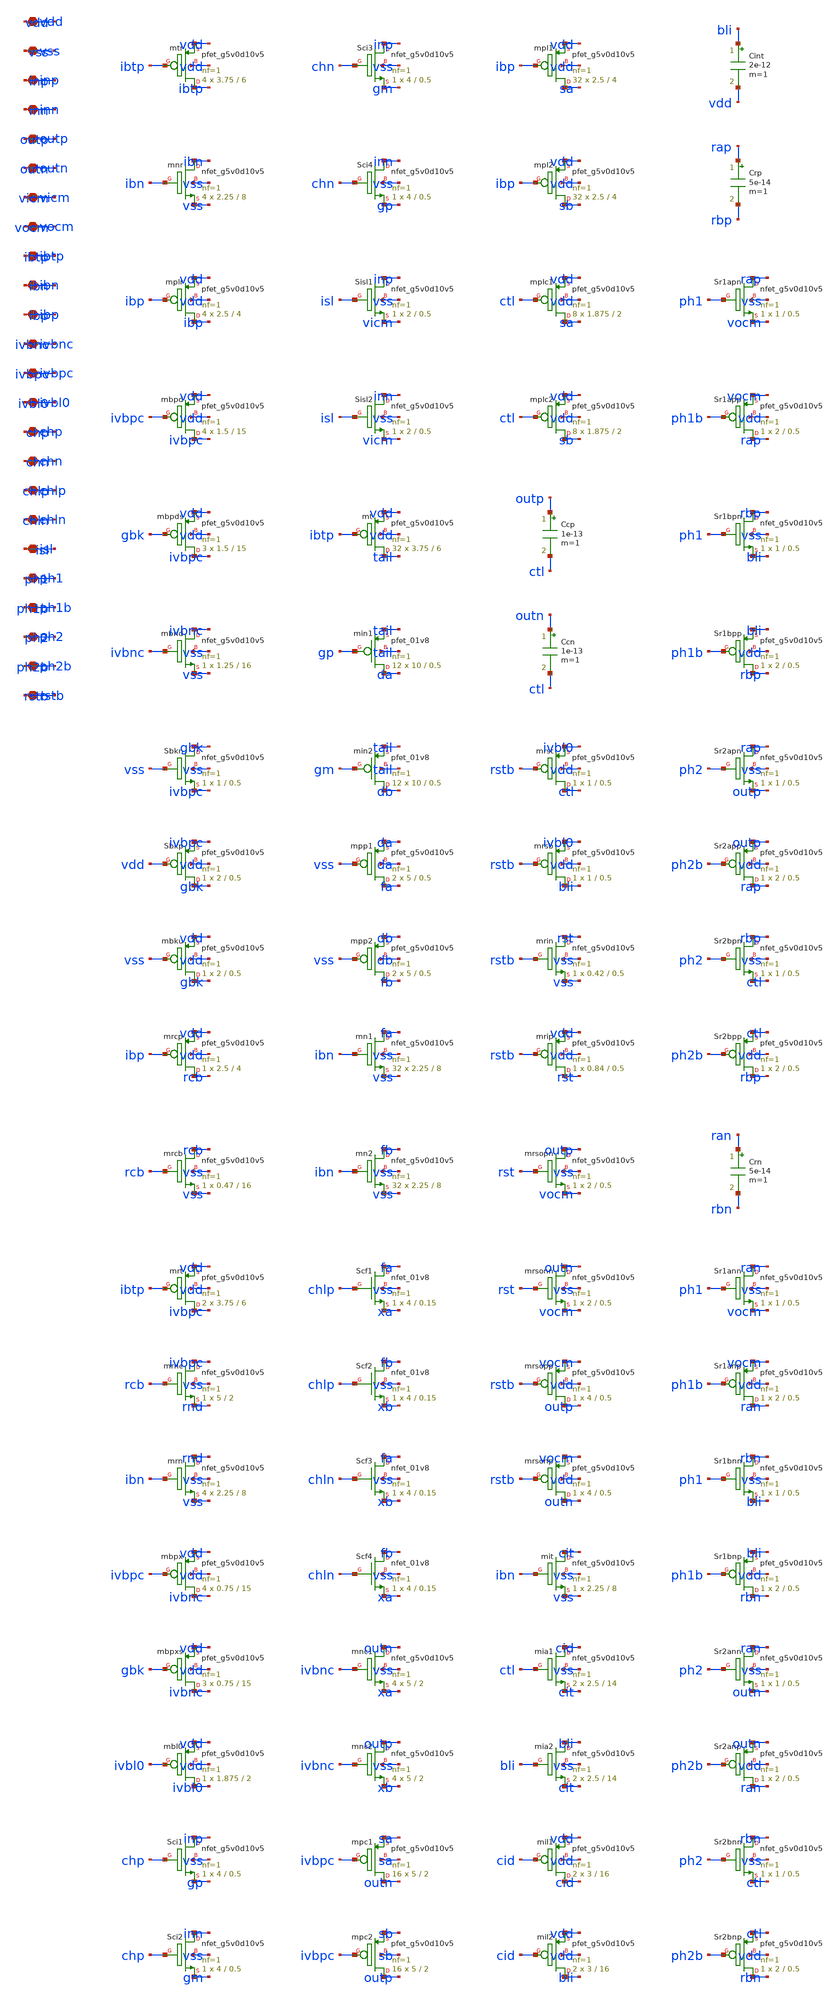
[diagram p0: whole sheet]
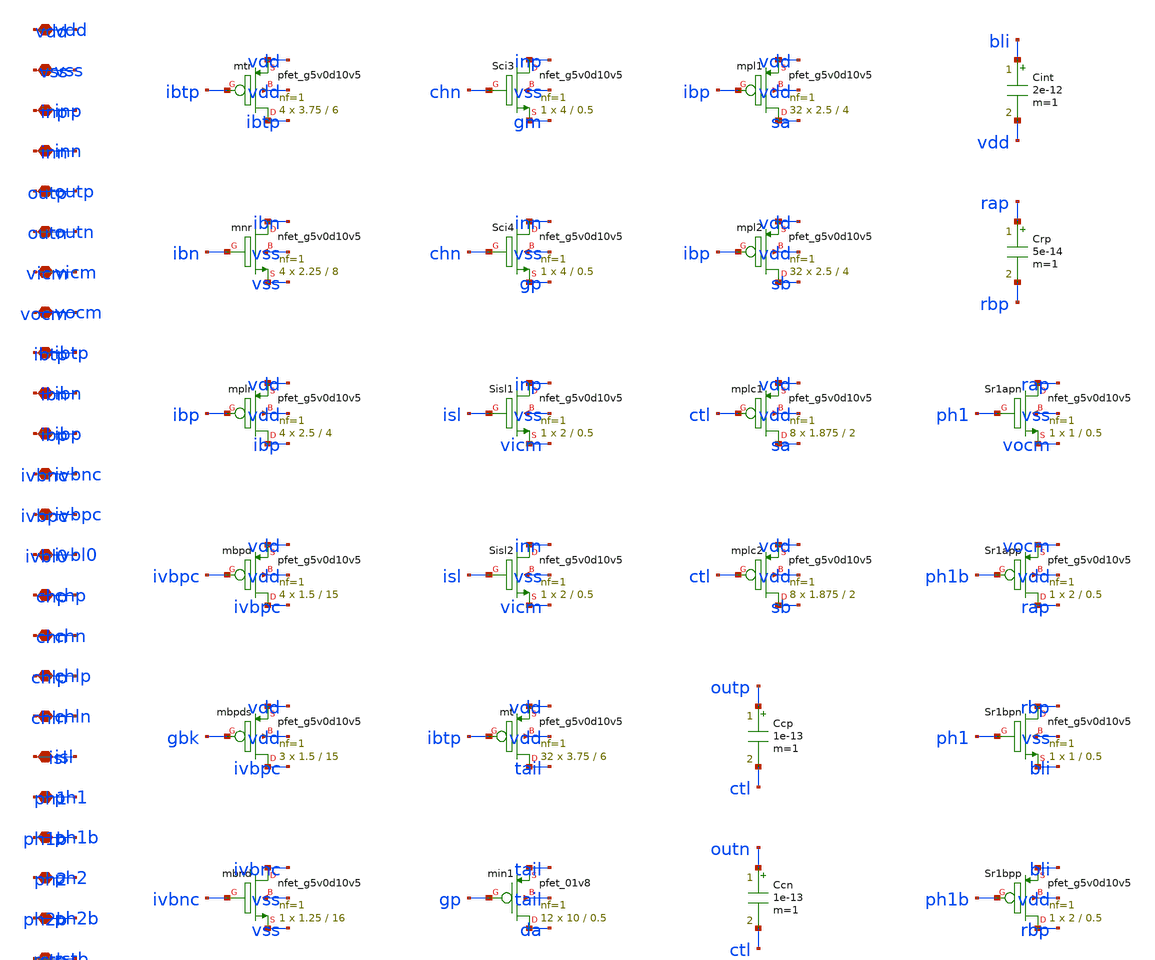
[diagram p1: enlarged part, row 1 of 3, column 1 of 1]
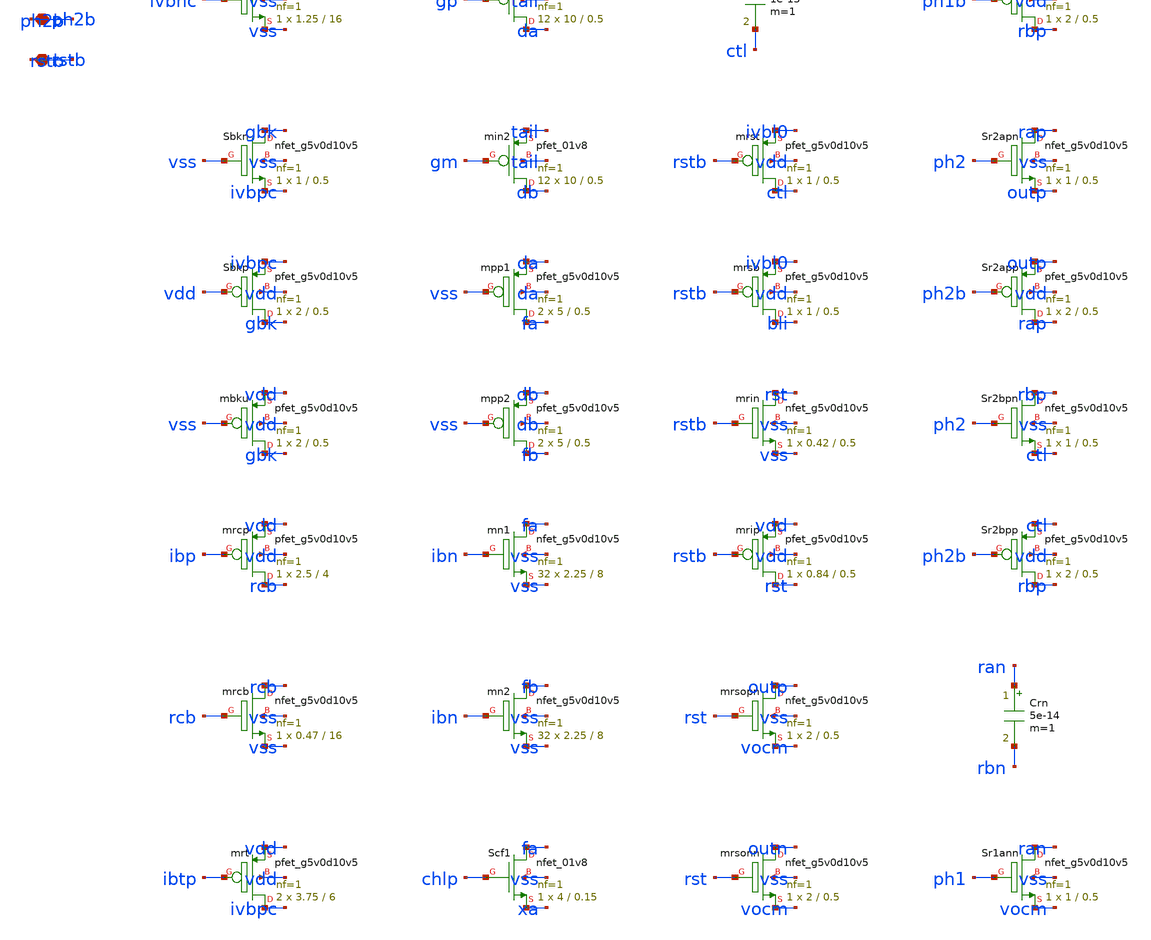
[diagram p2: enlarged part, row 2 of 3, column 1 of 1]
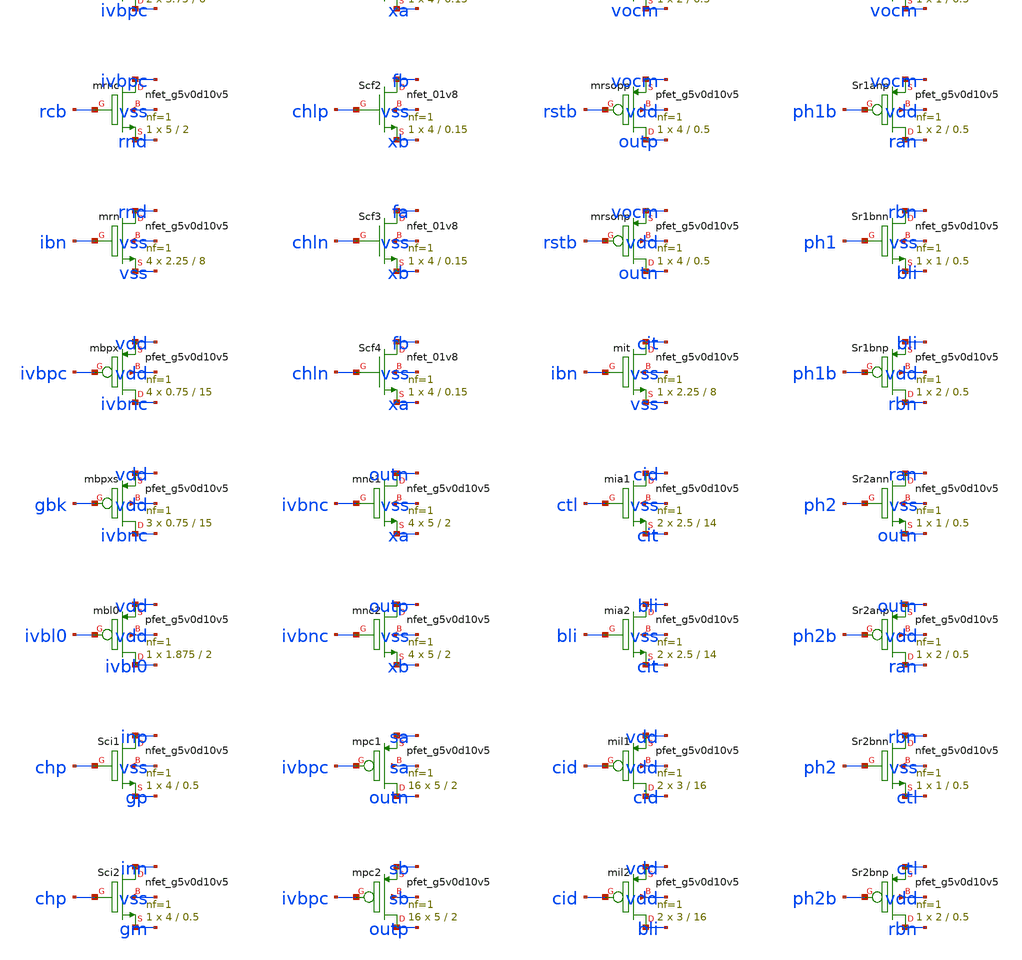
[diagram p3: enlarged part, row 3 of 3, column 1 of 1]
** sch_path: design/xschem/sch/ota1.sch
**.subckt ota1 vdd vss inp inn outp outn vicm vocm ibtp ibn ibp ivbnc ivbpc ivbl0 chp chn chlp chln
*+ isl ph1 ph1b ph2 ph2b rstb
*.iopin vdd
*.iopin vss
*.iopin inp
*.iopin inn
*.iopin outp
*.iopin outn
*.iopin vicm
*.iopin vocm
*.iopin ibtp
*.iopin ibn
*.iopin ibp
*.iopin ivbnc
*.iopin ivbpc
*.iopin ivbl0
*.iopin chp
*.iopin chn
*.iopin chlp
*.iopin chln
*.iopin isl
*.iopin ph1
*.iopin ph1b
*.iopin ph2
*.iopin ph2b
*.iopin rstb
Xmtr ibtp ibtp vdd vdd sky130_fd_pr__pfet_g5v0d10v5 L=6 W=3.75 nf=1 ad='int((1 + 1)/2) * 3.75 / 1 * 0.29'
+ as='int((1 + 2)/2) * 3.75 / 1 * 0.29' pd='2*int((1 + 1)/2) * (3.75 / 1 + 0.29)' ps='2*int((1 + 2)/2) * (3.75 / 1 + 0.29)'
+ nrd='0.29 / 3.75 ' nrs='0.29 / 3.75 ' sa=0 sb=0 sd=0 mult=4 m=4
Xmnr ibn ibn vss vss sky130_fd_pr__nfet_g5v0d10v5 L=8 W=2.25 nf=1 ad='int((1 + 1)/2) * 2.25 / 1 * 0.29'
+ as='int((1 + 2)/2) * 2.25 / 1 * 0.29' pd='2*int((1 + 1)/2) * (2.25 / 1 + 0.29)' ps='2*int((1 + 2)/2) * (2.25 / 1 + 0.29)'
+ nrd='0.29 / 2.25 ' nrs='0.29 / 2.25 ' sa=0 sb=0 sd=0 mult=4 m=4
Xmplr ibp ibp vdd vdd sky130_fd_pr__pfet_g5v0d10v5 L=4 W=2.5 nf=1 ad='int((1 + 1)/2) * 2.5 / 1 * 0.29'
+ as='int((1 + 2)/2) * 2.5 / 1 * 0.29' pd='2*int((1 + 1)/2) * (2.5 / 1 + 0.29)' ps='2*int((1 + 2)/2) * (2.5 / 1 + 0.29)'
+ nrd='0.29 / 2.5 ' nrs='0.29 / 2.5 ' sa=0 sb=0 sd=0 mult=4 m=4
Xmbpd ivbpc ivbpc vdd vdd sky130_fd_pr__pfet_g5v0d10v5 L=15 W=1.5 nf=1 ad='int((1 + 1)/2) * 1.5 / 1 * 0.29'
+ as='int((1 + 2)/2) * 1.5 / 1 * 0.29' pd='2*int((1 + 1)/2) * (1.5 / 1 + 0.29)' ps='2*int((1 + 2)/2) * (1.5 / 1 + 0.29)'
+ nrd='0.29 / 1.5 ' nrs='0.29 / 1.5 ' sa=0 sb=0 sd=0 mult=4 m=4
Xmbpds ivbpc gbk vdd vdd sky130_fd_pr__pfet_g5v0d10v5 L=15 W=1.5 nf=1 ad='int((1 + 1)/2) * 1.5 / 1 * 0.29'
+ as='int((1 + 2)/2) * 1.5 / 1 * 0.29' pd='2*int((1 + 1)/2) * (1.5 / 1 + 0.29)' ps='2*int((1 + 2)/2) * (1.5 / 1 + 0.29)'
+ nrd='0.29 / 1.5 ' nrs='0.29 / 1.5 ' sa=0 sb=0 sd=0 mult=3 m=3
Xmbnd ivbnc ivbnc vss vss sky130_fd_pr__nfet_g5v0d10v5 L=16 W=1.25 nf=1 ad='int((1 + 1)/2) * 1.25 / 1 * 0.29'
+ as='int((1 + 2)/2) * 1.25 / 1 * 0.29' pd='2*int((1 + 1)/2) * (1.25 / 1 + 0.29)' ps='2*int((1 + 2)/2) * (1.25 / 1 + 0.29)'
+ nrd='0.29 / 1.25 ' nrs='0.29 / 1.25 ' sa=0 sb=0 sd=0 mult=1 m=1
XSbkn gbk vss ivbpc vss sky130_fd_pr__nfet_g5v0d10v5 L=0.5 W=1 nf=1 ad='int((1 + 1)/2) * 1 / 1 * 0.29'
+ as='int((1 + 2)/2) * 1 / 1 * 0.29' pd='2*int((1 + 1)/2) * (1 / 1 + 0.29)' ps='2*int((1 + 2)/2) * (1 / 1 + 0.29)'
+ nrd='0.29 / 1 ' nrs='0.29 / 1 ' sa=0 sb=0 sd=0 mult=1 m=1
XSbkp gbk vdd ivbpc vdd sky130_fd_pr__pfet_g5v0d10v5 L=0.5 W=2 nf=1 ad='int((1 + 1)/2) * 2 / 1 * 0.29'
+ as='int((1 + 2)/2) * 2 / 1 * 0.29' pd='2*int((1 + 1)/2) * (2 / 1 + 0.29)' ps='2*int((1 + 2)/2) * (2 / 1 + 0.29)'
+ nrd='0.29 / 2 ' nrs='0.29 / 2 ' sa=0 sb=0 sd=0 mult=1 m=1
Xmbku gbk vss vdd vdd sky130_fd_pr__pfet_g5v0d10v5 L=0.5 W=2 nf=1 ad='int((1 + 1)/2) * 2 / 1 * 0.29'
+ as='int((1 + 2)/2) * 2 / 1 * 0.29' pd='2*int((1 + 1)/2) * (2 / 1 + 0.29)' ps='2*int((1 + 2)/2) * (2 / 1 + 0.29)'
+ nrd='0.29 / 2 ' nrs='0.29 / 2 ' sa=0 sb=0 sd=0 mult=1 m=1
Xmrcp rcb ibp vdd vdd sky130_fd_pr__pfet_g5v0d10v5 L=4 W=2.5 nf=1 ad='int((1 + 1)/2) * 2.5 / 1 * 0.29'
+ as='int((1 + 2)/2) * 2.5 / 1 * 0.29' pd='2*int((1 + 1)/2) * (2.5 / 1 + 0.29)' ps='2*int((1 + 2)/2) * (2.5 / 1 + 0.29)'
+ nrd='0.29 / 2.5 ' nrs='0.29 / 2.5 ' sa=0 sb=0 sd=0 mult=1 m=1
Xmrcb rcb rcb vss vss sky130_fd_pr__nfet_g5v0d10v5 L=16 W=0.47 nf=1 ad='int((1 + 1)/2) * 0.47 / 1 * 0.29'
+ as='int((1 + 2)/2) * 0.47 / 1 * 0.29' pd='2*int((1 + 1)/2) * (0.47 / 1 + 0.29)' ps='2*int((1 + 2)/2) * (0.47 / 1 + 0.29)'
+ nrd='0.29 / 0.47 ' nrs='0.29 / 0.47 ' sa=0 sb=0 sd=0 mult=1 m=1
Xmrt ivbpc ibtp vdd vdd sky130_fd_pr__pfet_g5v0d10v5 L=6 W=3.75 nf=1 ad='int((1 + 1)/2) * 3.75 / 1 * 0.29'
+ as='int((1 + 2)/2) * 3.75 / 1 * 0.29' pd='2*int((1 + 1)/2) * (3.75 / 1 + 0.29)' ps='2*int((1 + 2)/2) * (3.75 / 1 + 0.29)'
+ nrd='0.29 / 3.75 ' nrs='0.29 / 3.75 ' sa=0 sb=0 sd=0 mult=2 m=2
Xmrnc ivbpc rcb rnd vss sky130_fd_pr__nfet_g5v0d10v5 L=2 W=5 nf=1 ad='int((1 + 1)/2) * 5 / 1 * 0.29'
+ as='int((1 + 2)/2) * 5 / 1 * 0.29' pd='2*int((1 + 1)/2) * (5 / 1 + 0.29)' ps='2*int((1 + 2)/2) * (5 / 1 + 0.29)'
+ nrd='0.29 / 5 ' nrs='0.29 / 5 ' sa=0 sb=0 sd=0 mult=1 m=1
Xmrn rnd ibn vss vss sky130_fd_pr__nfet_g5v0d10v5 L=8 W=2.25 nf=1 ad='int((1 + 1)/2) * 2.25 / 1 * 0.29'
+ as='int((1 + 2)/2) * 2.25 / 1 * 0.29' pd='2*int((1 + 1)/2) * (2.25 / 1 + 0.29)' ps='2*int((1 + 2)/2) * (2.25 / 1 + 0.29)'
+ nrd='0.29 / 2.25 ' nrs='0.29 / 2.25 ' sa=0 sb=0 sd=0 mult=4 m=4
Xmbpx ivbnc ivbpc vdd vdd sky130_fd_pr__pfet_g5v0d10v5 L=15 W=0.75 nf=1 ad='int((1 + 1)/2) * 0.75 / 1 * 0.29'
+ as='int((1 + 2)/2) * 0.75 / 1 * 0.29' pd='2*int((1 + 1)/2) * (0.75 / 1 + 0.29)' ps='2*int((1 + 2)/2) * (0.75 / 1 + 0.29)'
+ nrd='0.29 / 0.75 ' nrs='0.29 / 0.75 ' sa=0 sb=0 sd=0 mult=4 m=4
Xmbpxs ivbnc gbk vdd vdd sky130_fd_pr__pfet_g5v0d10v5 L=15 W=0.75 nf=1 ad='int((1 + 1)/2) * 0.75 / 1 * 0.29'
+ as='int((1 + 2)/2) * 0.75 / 1 * 0.29' pd='2*int((1 + 1)/2) * (0.75 / 1 + 0.29)' ps='2*int((1 + 2)/2) * (0.75 / 1 + 0.29)'
+ nrd='0.29 / 0.75 ' nrs='0.29 / 0.75 ' sa=0 sb=0 sd=0 mult=3 m=3
Xmbl0 ivbl0 ivbl0 vdd vdd sky130_fd_pr__pfet_g5v0d10v5 L=2 W=1.875 nf=1 ad='int((1 + 1)/2) * 1.875 / 1 * 0.29'
+ as='int((1 + 2)/2) * 1.875 / 1 * 0.29' pd='2*int((1 + 1)/2) * (1.875 / 1 + 0.29)' ps='2*int((1 + 2)/2) * (1.875 / 1 + 0.29)'
+ nrd='0.29 / 1.875 ' nrs='0.29 / 1.875 ' sa=0 sb=0 sd=0 mult=1 m=1
XSci1 inp chp gp vss sky130_fd_pr__nfet_g5v0d10v5 L=0.5 W=4 nf=1 ad='int((1 + 1)/2) * 4 / 1 * 0.29' as='int((1 + 2)/2) * 4 / 1 * 0.29'
+ pd='2*int((1 + 1)/2) * (4 / 1 + 0.29)' ps='2*int((1 + 2)/2) * (4 / 1 + 0.29)' nrd='0.29 / 4 ' nrs='0.29 / 4 '
+ sa=0 sb=0 sd=0 mult=1 m=1
XSci2 inn chp gm vss sky130_fd_pr__nfet_g5v0d10v5 L=0.5 W=4 nf=1 ad='int((1 + 1)/2) * 4 / 1 * 0.29' as='int((1 + 2)/2) * 4 / 1 * 0.29'
+ pd='2*int((1 + 1)/2) * (4 / 1 + 0.29)' ps='2*int((1 + 2)/2) * (4 / 1 + 0.29)' nrd='0.29 / 4 ' nrs='0.29 / 4 '
+ sa=0 sb=0 sd=0 mult=1 m=1
XSci3 inp chn gm vss sky130_fd_pr__nfet_g5v0d10v5 L=0.5 W=4 nf=1 ad='int((1 + 1)/2) * 4 / 1 * 0.29' as='int((1 + 2)/2) * 4 / 1 * 0.29'
+ pd='2*int((1 + 1)/2) * (4 / 1 + 0.29)' ps='2*int((1 + 2)/2) * (4 / 1 + 0.29)' nrd='0.29 / 4 ' nrs='0.29 / 4 '
+ sa=0 sb=0 sd=0 mult=1 m=1
XSci4 inn chn gp vss sky130_fd_pr__nfet_g5v0d10v5 L=0.5 W=4 nf=1 ad='int((1 + 1)/2) * 4 / 1 * 0.29' as='int((1 + 2)/2) * 4 / 1 * 0.29'
+ pd='2*int((1 + 1)/2) * (4 / 1 + 0.29)' ps='2*int((1 + 2)/2) * (4 / 1 + 0.29)' nrd='0.29 / 4 ' nrs='0.29 / 4 '
+ sa=0 sb=0 sd=0 mult=1 m=1
XSisl1 inp isl vicm vss sky130_fd_pr__nfet_g5v0d10v5 L=0.5 W=2 nf=1 ad='int((1 + 1)/2) * 2 / 1 * 0.29'
+ as='int((1 + 2)/2) * 2 / 1 * 0.29' pd='2*int((1 + 1)/2) * (2 / 1 + 0.29)' ps='2*int((1 + 2)/2) * (2 / 1 + 0.29)'
+ nrd='0.29 / 2 ' nrs='0.29 / 2 ' sa=0 sb=0 sd=0 mult=1 m=1
XSisl2 inn isl vicm vss sky130_fd_pr__nfet_g5v0d10v5 L=0.5 W=2 nf=1 ad='int((1 + 1)/2) * 2 / 1 * 0.29'
+ as='int((1 + 2)/2) * 2 / 1 * 0.29' pd='2*int((1 + 1)/2) * (2 / 1 + 0.29)' ps='2*int((1 + 2)/2) * (2 / 1 + 0.29)'
+ nrd='0.29 / 2 ' nrs='0.29 / 2 ' sa=0 sb=0 sd=0 mult=1 m=1
Xmt tail ibtp vdd vdd sky130_fd_pr__pfet_g5v0d10v5 L=6 W=3.75 nf=1 ad='int((1 + 1)/2) * 3.75 / 1 * 0.29'
+ as='int((1 + 2)/2) * 3.75 / 1 * 0.29' pd='2*int((1 + 1)/2) * (3.75 / 1 + 0.29)' ps='2*int((1 + 2)/2) * (3.75 / 1 + 0.29)'
+ nrd='0.29 / 3.75 ' nrs='0.29 / 3.75 ' sa=0 sb=0 sd=0 mult=32 m=32
Xmin1 da gp tail tail sky130_fd_pr__pfet_01v8 L=0.5 W=10 nf=1 ad='int((nf+1)/2) * W/nf * 0.29' as='int((nf+2)/2) * W/nf * 0.29'
+ pd='2*int((nf+1)/2) * (W/nf + 0.29)' ps='2*int((nf+2)/2) * (W/nf + 0.29)' nrd='0.29 / W' nrs='0.29 / W'
+ sa=0 sb=0 sd=0 mult=12 m=12
Xmin2 db gm tail tail sky130_fd_pr__pfet_01v8 L=0.5 W=10 nf=1 ad='int((nf+1)/2) * W/nf * 0.29' as='int((nf+2)/2) * W/nf * 0.29'
+ pd='2*int((nf+1)/2) * (W/nf + 0.29)' ps='2*int((nf+2)/2) * (W/nf + 0.29)' nrd='0.29 / W' nrs='0.29 / W'
+ sa=0 sb=0 sd=0 mult=12 m=12
Xmpp1 fa vss da da sky130_fd_pr__pfet_g5v0d10v5 L=0.5 W=5 nf=1 ad='int((1 + 1)/2) * 5 / 1 * 0.29' as='int((1 + 2)/2) * 5 / 1 * 0.29'
+ pd='2*int((1 + 1)/2) * (5 / 1 + 0.29)' ps='2*int((1 + 2)/2) * (5 / 1 + 0.29)' nrd='0.29 / 5 ' nrs='0.29 / 5 '
+ sa=0 sb=0 sd=0 mult=2 m=2
Xmpp2 fb vss db db sky130_fd_pr__pfet_g5v0d10v5 L=0.5 W=5 nf=1 ad='int((1 + 1)/2) * 5 / 1 * 0.29' as='int((1 + 2)/2) * 5 / 1 * 0.29'
+ pd='2*int((1 + 1)/2) * (5 / 1 + 0.29)' ps='2*int((1 + 2)/2) * (5 / 1 + 0.29)' nrd='0.29 / 5 ' nrs='0.29 / 5 '
+ sa=0 sb=0 sd=0 mult=2 m=2
Xmn1 fa ibn vss vss sky130_fd_pr__nfet_g5v0d10v5 L=8 W=2.25 nf=1 ad='int((1 + 1)/2) * 2.25 / 1 * 0.29'
+ as='int((1 + 2)/2) * 2.25 / 1 * 0.29' pd='2*int((1 + 1)/2) * (2.25 / 1 + 0.29)' ps='2*int((1 + 2)/2) * (2.25 / 1 + 0.29)'
+ nrd='0.29 / 2.25 ' nrs='0.29 / 2.25 ' sa=0 sb=0 sd=0 mult=32 m=32
Xmn2 fb ibn vss vss sky130_fd_pr__nfet_g5v0d10v5 L=8 W=2.25 nf=1 ad='int((1 + 1)/2) * 2.25 / 1 * 0.29'
+ as='int((1 + 2)/2) * 2.25 / 1 * 0.29' pd='2*int((1 + 1)/2) * (2.25 / 1 + 0.29)' ps='2*int((1 + 2)/2) * (2.25 / 1 + 0.29)'
+ nrd='0.29 / 2.25 ' nrs='0.29 / 2.25 ' sa=0 sb=0 sd=0 mult=32 m=32
XScf1 fa chlp xa vss sky130_fd_pr__nfet_01v8 L=0.15 W=4 nf=1 ad='int((1 + 1)/2) * 4 / 1 * 0.29' as='int((1 + 2)/2) * 4 / 1 * 0.29'
+ pd='2*int((1 + 1)/2) * (4 / 1 + 0.29)' ps='2*int((1 + 2)/2) * (4 / 1 + 0.29)' nrd='0.29 / 4 ' nrs='0.29 / 4 '
+ sa=0 sb=0 sd=0 mult=1 m=1
XScf2 fb chlp xb vss sky130_fd_pr__nfet_01v8 L=0.15 W=4 nf=1 ad='int((1 + 1)/2) * 4 / 1 * 0.29' as='int((1 + 2)/2) * 4 / 1 * 0.29'
+ pd='2*int((1 + 1)/2) * (4 / 1 + 0.29)' ps='2*int((1 + 2)/2) * (4 / 1 + 0.29)' nrd='0.29 / 4 ' nrs='0.29 / 4 '
+ sa=0 sb=0 sd=0 mult=1 m=1
XScf3 fa chln xb vss sky130_fd_pr__nfet_01v8 L=0.15 W=4 nf=1 ad='int((1 + 1)/2) * 4 / 1 * 0.29' as='int((1 + 2)/2) * 4 / 1 * 0.29'
+ pd='2*int((1 + 1)/2) * (4 / 1 + 0.29)' ps='2*int((1 + 2)/2) * (4 / 1 + 0.29)' nrd='0.29 / 4 ' nrs='0.29 / 4 '
+ sa=0 sb=0 sd=0 mult=1 m=1
XScf4 fb chln xa vss sky130_fd_pr__nfet_01v8 L=0.15 W=4 nf=1 ad='int((1 + 1)/2) * 4 / 1 * 0.29' as='int((1 + 2)/2) * 4 / 1 * 0.29'
+ pd='2*int((1 + 1)/2) * (4 / 1 + 0.29)' ps='2*int((1 + 2)/2) * (4 / 1 + 0.29)' nrd='0.29 / 4 ' nrs='0.29 / 4 '
+ sa=0 sb=0 sd=0 mult=1 m=1
Xmnc1 outn ivbnc xa vss sky130_fd_pr__nfet_g5v0d10v5 L=2 W=5 nf=1 ad='int((1 + 1)/2) * 5 / 1 * 0.29'
+ as='int((1 + 2)/2) * 5 / 1 * 0.29' pd='2*int((1 + 1)/2) * (5 / 1 + 0.29)' ps='2*int((1 + 2)/2) * (5 / 1 + 0.29)'
+ nrd='0.29 / 5 ' nrs='0.29 / 5 ' sa=0 sb=0 sd=0 mult=4 m=4
Xmnc2 outp ivbnc xb vss sky130_fd_pr__nfet_g5v0d10v5 L=2 W=5 nf=1 ad='int((1 + 1)/2) * 5 / 1 * 0.29'
+ as='int((1 + 2)/2) * 5 / 1 * 0.29' pd='2*int((1 + 1)/2) * (5 / 1 + 0.29)' ps='2*int((1 + 2)/2) * (5 / 1 + 0.29)'
+ nrd='0.29 / 5 ' nrs='0.29 / 5 ' sa=0 sb=0 sd=0 mult=4 m=4
Xmpc1 outn ivbpc sa sa sky130_fd_pr__pfet_g5v0d10v5 L=2 W=5 nf=1 ad='int((1 + 1)/2) * 5 / 1 * 0.29' as='int((1 + 2)/2) * 5 / 1 * 0.29'
+ pd='2*int((1 + 1)/2) * (5 / 1 + 0.29)' ps='2*int((1 + 2)/2) * (5 / 1 + 0.29)' nrd='0.29 / 5 ' nrs='0.29 / 5 '
+ sa=0 sb=0 sd=0 mult=16 m=16
Xmpc2 outp ivbpc sb sb sky130_fd_pr__pfet_g5v0d10v5 L=2 W=5 nf=1 ad='int((1 + 1)/2) * 5 / 1 * 0.29' as='int((1 + 2)/2) * 5 / 1 * 0.29'
+ pd='2*int((1 + 1)/2) * (5 / 1 + 0.29)' ps='2*int((1 + 2)/2) * (5 / 1 + 0.29)' nrd='0.29 / 5 ' nrs='0.29 / 5 '
+ sa=0 sb=0 sd=0 mult=16 m=16
Xmpl1 sa ibp vdd vdd sky130_fd_pr__pfet_g5v0d10v5 L=4 W=2.5 nf=1 ad='int((1 + 1)/2) * 2.5 / 1 * 0.29'
+ as='int((1 + 2)/2) * 2.5 / 1 * 0.29' pd='2*int((1 + 1)/2) * (2.5 / 1 + 0.29)' ps='2*int((1 + 2)/2) * (2.5 / 1 + 0.29)'
+ nrd='0.29 / 2.5 ' nrs='0.29 / 2.5 ' sa=0 sb=0 sd=0 mult=32 m=32
Xmpl2 sb ibp vdd vdd sky130_fd_pr__pfet_g5v0d10v5 L=4 W=2.5 nf=1 ad='int((1 + 1)/2) * 2.5 / 1 * 0.29'
+ as='int((1 + 2)/2) * 2.5 / 1 * 0.29' pd='2*int((1 + 1)/2) * (2.5 / 1 + 0.29)' ps='2*int((1 + 2)/2) * (2.5 / 1 + 0.29)'
+ nrd='0.29 / 2.5 ' nrs='0.29 / 2.5 ' sa=0 sb=0 sd=0 mult=32 m=32
Xmplc1 sa ctl vdd vdd sky130_fd_pr__pfet_g5v0d10v5 L=2 W=1.875 nf=1 ad='int((1 + 1)/2) * 1.875 / 1 * 0.29'
+ as='int((1 + 2)/2) * 1.875 / 1 * 0.29' pd='2*int((1 + 1)/2) * (1.875 / 1 + 0.29)' ps='2*int((1 + 2)/2) * (1.875 / 1 + 0.29)'
+ nrd='0.29 / 1.875 ' nrs='0.29 / 1.875 ' sa=0 sb=0 sd=0 mult=8 m=8
Xmplc2 sb ctl vdd vdd sky130_fd_pr__pfet_g5v0d10v5 L=2 W=1.875 nf=1 ad='int((1 + 1)/2) * 1.875 / 1 * 0.29'
+ as='int((1 + 2)/2) * 1.875 / 1 * 0.29' pd='2*int((1 + 1)/2) * (1.875 / 1 + 0.29)' ps='2*int((1 + 2)/2) * (1.875 / 1 + 0.29)'
+ nrd='0.29 / 1.875 ' nrs='0.29 / 1.875 ' sa=0 sb=0 sd=0 mult=8 m=8
Ccp outp ctl 1e-13 m=1
Ccn outn ctl 1e-13 m=1
Xmrst ctl rstb ivbl0 vdd sky130_fd_pr__pfet_g5v0d10v5 L=0.5 W=1 nf=1 ad='int((1 + 1)/2) * 1 / 1 * 0.29'
+ as='int((1 + 2)/2) * 1 / 1 * 0.29' pd='2*int((1 + 1)/2) * (1 / 1 + 0.29)' ps='2*int((1 + 2)/2) * (1 / 1 + 0.29)'
+ nrd='0.29 / 1 ' nrs='0.29 / 1 ' sa=0 sb=0 sd=0 mult=1 m=1
Xmrsb bli rstb ivbl0 vdd sky130_fd_pr__pfet_g5v0d10v5 L=0.5 W=1 nf=1 ad='int((1 + 1)/2) * 1 / 1 * 0.29'
+ as='int((1 + 2)/2) * 1 / 1 * 0.29' pd='2*int((1 + 1)/2) * (1 / 1 + 0.29)' ps='2*int((1 + 2)/2) * (1 / 1 + 0.29)'
+ nrd='0.29 / 1 ' nrs='0.29 / 1 ' sa=0 sb=0 sd=0 mult=1 m=1
Xmrin rst rstb vss vss sky130_fd_pr__nfet_g5v0d10v5 L=0.5 W=0.42 nf=1 ad='int((1 + 1)/2) * 0.42 / 1 * 0.29'
+ as='int((1 + 2)/2) * 0.42 / 1 * 0.29' pd='2*int((1 + 1)/2) * (0.42 / 1 + 0.29)' ps='2*int((1 + 2)/2) * (0.42 / 1 + 0.29)'
+ nrd='0.29 / 0.42 ' nrs='0.29 / 0.42 ' sa=0 sb=0 sd=0 mult=1 m=1
Xmrip rst rstb vdd vdd sky130_fd_pr__pfet_g5v0d10v5 L=0.5 W=0.84 nf=1 ad='int((1 + 1)/2) * 0.84 / 1 * 0.29'
+ as='int((1 + 2)/2) * 0.84 / 1 * 0.29' pd='2*int((1 + 1)/2) * (0.84 / 1 + 0.29)' ps='2*int((1 + 2)/2) * (0.84 / 1 + 0.29)'
+ nrd='0.29 / 0.84 ' nrs='0.29 / 0.84 ' sa=0 sb=0 sd=0 mult=1 m=1
Xmrsopn outp rst vocm vss sky130_fd_pr__nfet_g5v0d10v5 L=0.5 W=2 nf=1 ad='int((1 + 1)/2) * 2 / 1 * 0.29'
+ as='int((1 + 2)/2) * 2 / 1 * 0.29' pd='2*int((1 + 1)/2) * (2 / 1 + 0.29)' ps='2*int((1 + 2)/2) * (2 / 1 + 0.29)'
+ nrd='0.29 / 2 ' nrs='0.29 / 2 ' sa=0 sb=0 sd=0 mult=1 m=1
Xmrsonn outn rst vocm vss sky130_fd_pr__nfet_g5v0d10v5 L=0.5 W=2 nf=1 ad='int((1 + 1)/2) * 2 / 1 * 0.29'
+ as='int((1 + 2)/2) * 2 / 1 * 0.29' pd='2*int((1 + 1)/2) * (2 / 1 + 0.29)' ps='2*int((1 + 2)/2) * (2 / 1 + 0.29)'
+ nrd='0.29 / 2 ' nrs='0.29 / 2 ' sa=0 sb=0 sd=0 mult=1 m=1
Xmrsopp outp rstb vocm vdd sky130_fd_pr__pfet_g5v0d10v5 L=0.5 W=4 nf=1 ad='int((1 + 1)/2) * 4 / 1 * 0.29'
+ as='int((1 + 2)/2) * 4 / 1 * 0.29' pd='2*int((1 + 1)/2) * (4 / 1 + 0.29)' ps='2*int((1 + 2)/2) * (4 / 1 + 0.29)'
+ nrd='0.29 / 4 ' nrs='0.29 / 4 ' sa=0 sb=0 sd=0 mult=1 m=1
Xmrsonp outn rstb vocm vdd sky130_fd_pr__pfet_g5v0d10v5 L=0.5 W=4 nf=1 ad='int((1 + 1)/2) * 4 / 1 * 0.29'
+ as='int((1 + 2)/2) * 4 / 1 * 0.29' pd='2*int((1 + 1)/2) * (4 / 1 + 0.29)' ps='2*int((1 + 2)/2) * (4 / 1 + 0.29)'
+ nrd='0.29 / 4 ' nrs='0.29 / 4 ' sa=0 sb=0 sd=0 mult=1 m=1
Xmit cit ibn vss vss sky130_fd_pr__nfet_g5v0d10v5 L=8 W=2.25 nf=1 ad='int((1 + 1)/2) * 2.25 / 1 * 0.29'
+ as='int((1 + 2)/2) * 2.25 / 1 * 0.29' pd='2*int((1 + 1)/2) * (2.25 / 1 + 0.29)' ps='2*int((1 + 2)/2) * (2.25 / 1 + 0.29)'
+ nrd='0.29 / 2.25 ' nrs='0.29 / 2.25 ' sa=0 sb=0 sd=0 mult=1 m=1
Xmia1 cid ctl cit vss sky130_fd_pr__nfet_g5v0d10v5 L=14 W=2.5 nf=1 ad='int((1 + 1)/2) * 2.5 / 1 * 0.29'
+ as='int((1 + 2)/2) * 2.5 / 1 * 0.29' pd='2*int((1 + 1)/2) * (2.5 / 1 + 0.29)' ps='2*int((1 + 2)/2) * (2.5 / 1 + 0.29)'
+ nrd='0.29 / 2.5 ' nrs='0.29 / 2.5 ' sa=0 sb=0 sd=0 mult=2 m=2
Xmia2 bli bli cit vss sky130_fd_pr__nfet_g5v0d10v5 L=14 W=2.5 nf=1 ad='int((1 + 1)/2) * 2.5 / 1 * 0.29'
+ as='int((1 + 2)/2) * 2.5 / 1 * 0.29' pd='2*int((1 + 1)/2) * (2.5 / 1 + 0.29)' ps='2*int((1 + 2)/2) * (2.5 / 1 + 0.29)'
+ nrd='0.29 / 2.5 ' nrs='0.29 / 2.5 ' sa=0 sb=0 sd=0 mult=2 m=2
Xmil1 cid cid vdd vdd sky130_fd_pr__pfet_g5v0d10v5 L=16 W=3 nf=1 ad='int((1 + 1)/2) * 3 / 1 * 0.29' as='int((1 + 2)/2) * 3 / 1 * 0.29'
+ pd='2*int((1 + 1)/2) * (3 / 1 + 0.29)' ps='2*int((1 + 2)/2) * (3 / 1 + 0.29)' nrd='0.29 / 3 ' nrs='0.29 / 3 '
+ sa=0 sb=0 sd=0 mult=2 m=2
Xmil2 bli cid vdd vdd sky130_fd_pr__pfet_g5v0d10v5 L=16 W=3 nf=1 ad='int((1 + 1)/2) * 3 / 1 * 0.29' as='int((1 + 2)/2) * 3 / 1 * 0.29'
+ pd='2*int((1 + 1)/2) * (3 / 1 + 0.29)' ps='2*int((1 + 2)/2) * (3 / 1 + 0.29)' nrd='0.29 / 3 ' nrs='0.29 / 3 '
+ sa=0 sb=0 sd=0 mult=2 m=2
Cint bli vdd 2e-12 m=1
Crp rap rbp 5e-14 m=1
XSr1apn rap ph1 vocm vss sky130_fd_pr__nfet_g5v0d10v5 L=0.5 W=1 nf=1 ad='int((1 + 1)/2) * 1 / 1 * 0.29'
+ as='int((1 + 2)/2) * 1 / 1 * 0.29' pd='2*int((1 + 1)/2) * (1 / 1 + 0.29)' ps='2*int((1 + 2)/2) * (1 / 1 + 0.29)'
+ nrd='0.29 / 1 ' nrs='0.29 / 1 ' sa=0 sb=0 sd=0 mult=1 m=1
XSr1app rap ph1b vocm vdd sky130_fd_pr__pfet_g5v0d10v5 L=0.5 W=2 nf=1 ad='int((1 + 1)/2) * 2 / 1 * 0.29'
+ as='int((1 + 2)/2) * 2 / 1 * 0.29' pd='2*int((1 + 1)/2) * (2 / 1 + 0.29)' ps='2*int((1 + 2)/2) * (2 / 1 + 0.29)'
+ nrd='0.29 / 2 ' nrs='0.29 / 2 ' sa=0 sb=0 sd=0 mult=1 m=1
XSr1bpn rbp ph1 bli vss sky130_fd_pr__nfet_g5v0d10v5 L=0.5 W=1 nf=1 ad='int((1 + 1)/2) * 1 / 1 * 0.29'
+ as='int((1 + 2)/2) * 1 / 1 * 0.29' pd='2*int((1 + 1)/2) * (1 / 1 + 0.29)' ps='2*int((1 + 2)/2) * (1 / 1 + 0.29)'
+ nrd='0.29 / 1 ' nrs='0.29 / 1 ' sa=0 sb=0 sd=0 mult=1 m=1
XSr1bpp rbp ph1b bli vdd sky130_fd_pr__pfet_g5v0d10v5 L=0.5 W=2 nf=1 ad='int((1 + 1)/2) * 2 / 1 * 0.29'
+ as='int((1 + 2)/2) * 2 / 1 * 0.29' pd='2*int((1 + 1)/2) * (2 / 1 + 0.29)' ps='2*int((1 + 2)/2) * (2 / 1 + 0.29)'
+ nrd='0.29 / 2 ' nrs='0.29 / 2 ' sa=0 sb=0 sd=0 mult=1 m=1
XSr2apn rap ph2 outp vss sky130_fd_pr__nfet_g5v0d10v5 L=0.5 W=1 nf=1 ad='int((1 + 1)/2) * 1 / 1 * 0.29'
+ as='int((1 + 2)/2) * 1 / 1 * 0.29' pd='2*int((1 + 1)/2) * (1 / 1 + 0.29)' ps='2*int((1 + 2)/2) * (1 / 1 + 0.29)'
+ nrd='0.29 / 1 ' nrs='0.29 / 1 ' sa=0 sb=0 sd=0 mult=1 m=1
XSr2app rap ph2b outp vdd sky130_fd_pr__pfet_g5v0d10v5 L=0.5 W=2 nf=1 ad='int((1 + 1)/2) * 2 / 1 * 0.29'
+ as='int((1 + 2)/2) * 2 / 1 * 0.29' pd='2*int((1 + 1)/2) * (2 / 1 + 0.29)' ps='2*int((1 + 2)/2) * (2 / 1 + 0.29)'
+ nrd='0.29 / 2 ' nrs='0.29 / 2 ' sa=0 sb=0 sd=0 mult=1 m=1
XSr2bpn rbp ph2 ctl vss sky130_fd_pr__nfet_g5v0d10v5 L=0.5 W=1 nf=1 ad='int((1 + 1)/2) * 1 / 1 * 0.29'
+ as='int((1 + 2)/2) * 1 / 1 * 0.29' pd='2*int((1 + 1)/2) * (1 / 1 + 0.29)' ps='2*int((1 + 2)/2) * (1 / 1 + 0.29)'
+ nrd='0.29 / 1 ' nrs='0.29 / 1 ' sa=0 sb=0 sd=0 mult=1 m=1
XSr2bpp rbp ph2b ctl vdd sky130_fd_pr__pfet_g5v0d10v5 L=0.5 W=2 nf=1 ad='int((1 + 1)/2) * 2 / 1 * 0.29'
+ as='int((1 + 2)/2) * 2 / 1 * 0.29' pd='2*int((1 + 1)/2) * (2 / 1 + 0.29)' ps='2*int((1 + 2)/2) * (2 / 1 + 0.29)'
+ nrd='0.29 / 2 ' nrs='0.29 / 2 ' sa=0 sb=0 sd=0 mult=1 m=1
Crn ran rbn 5e-14 m=1
XSr1ann ran ph1 vocm vss sky130_fd_pr__nfet_g5v0d10v5 L=0.5 W=1 nf=1 ad='int((1 + 1)/2) * 1 / 1 * 0.29'
+ as='int((1 + 2)/2) * 1 / 1 * 0.29' pd='2*int((1 + 1)/2) * (1 / 1 + 0.29)' ps='2*int((1 + 2)/2) * (1 / 1 + 0.29)'
+ nrd='0.29 / 1 ' nrs='0.29 / 1 ' sa=0 sb=0 sd=0 mult=1 m=1
XSr1anp ran ph1b vocm vdd sky130_fd_pr__pfet_g5v0d10v5 L=0.5 W=2 nf=1 ad='int((1 + 1)/2) * 2 / 1 * 0.29'
+ as='int((1 + 2)/2) * 2 / 1 * 0.29' pd='2*int((1 + 1)/2) * (2 / 1 + 0.29)' ps='2*int((1 + 2)/2) * (2 / 1 + 0.29)'
+ nrd='0.29 / 2 ' nrs='0.29 / 2 ' sa=0 sb=0 sd=0 mult=1 m=1
XSr1bnn rbn ph1 bli vss sky130_fd_pr__nfet_g5v0d10v5 L=0.5 W=1 nf=1 ad='int((1 + 1)/2) * 1 / 1 * 0.29'
+ as='int((1 + 2)/2) * 1 / 1 * 0.29' pd='2*int((1 + 1)/2) * (1 / 1 + 0.29)' ps='2*int((1 + 2)/2) * (1 / 1 + 0.29)'
+ nrd='0.29 / 1 ' nrs='0.29 / 1 ' sa=0 sb=0 sd=0 mult=1 m=1
XSr1bnp rbn ph1b bli vdd sky130_fd_pr__pfet_g5v0d10v5 L=0.5 W=2 nf=1 ad='int((1 + 1)/2) * 2 / 1 * 0.29'
+ as='int((1 + 2)/2) * 2 / 1 * 0.29' pd='2*int((1 + 1)/2) * (2 / 1 + 0.29)' ps='2*int((1 + 2)/2) * (2 / 1 + 0.29)'
+ nrd='0.29 / 2 ' nrs='0.29 / 2 ' sa=0 sb=0 sd=0 mult=1 m=1
XSr2ann ran ph2 outn vss sky130_fd_pr__nfet_g5v0d10v5 L=0.5 W=1 nf=1 ad='int((1 + 1)/2) * 1 / 1 * 0.29'
+ as='int((1 + 2)/2) * 1 / 1 * 0.29' pd='2*int((1 + 1)/2) * (1 / 1 + 0.29)' ps='2*int((1 + 2)/2) * (1 / 1 + 0.29)'
+ nrd='0.29 / 1 ' nrs='0.29 / 1 ' sa=0 sb=0 sd=0 mult=1 m=1
XSr2anp ran ph2b outn vdd sky130_fd_pr__pfet_g5v0d10v5 L=0.5 W=2 nf=1 ad='int((1 + 1)/2) * 2 / 1 * 0.29'
+ as='int((1 + 2)/2) * 2 / 1 * 0.29' pd='2*int((1 + 1)/2) * (2 / 1 + 0.29)' ps='2*int((1 + 2)/2) * (2 / 1 + 0.29)'
+ nrd='0.29 / 2 ' nrs='0.29 / 2 ' sa=0 sb=0 sd=0 mult=1 m=1
XSr2bnn rbn ph2 ctl vss sky130_fd_pr__nfet_g5v0d10v5 L=0.5 W=1 nf=1 ad='int((1 + 1)/2) * 1 / 1 * 0.29'
+ as='int((1 + 2)/2) * 1 / 1 * 0.29' pd='2*int((1 + 1)/2) * (1 / 1 + 0.29)' ps='2*int((1 + 2)/2) * (1 / 1 + 0.29)'
+ nrd='0.29 / 1 ' nrs='0.29 / 1 ' sa=0 sb=0 sd=0 mult=1 m=1
XSr2bnp rbn ph2b ctl vdd sky130_fd_pr__pfet_g5v0d10v5 L=0.5 W=2 nf=1 ad='int((1 + 1)/2) * 2 / 1 * 0.29'
+ as='int((1 + 2)/2) * 2 / 1 * 0.29' pd='2*int((1 + 1)/2) * (2 / 1 + 0.29)' ps='2*int((1 + 2)/2) * (2 / 1 + 0.29)'
+ nrd='0.29 / 2 ' nrs='0.29 / 2 ' sa=0 sb=0 sd=0 mult=1 m=1
**.ends
.end
